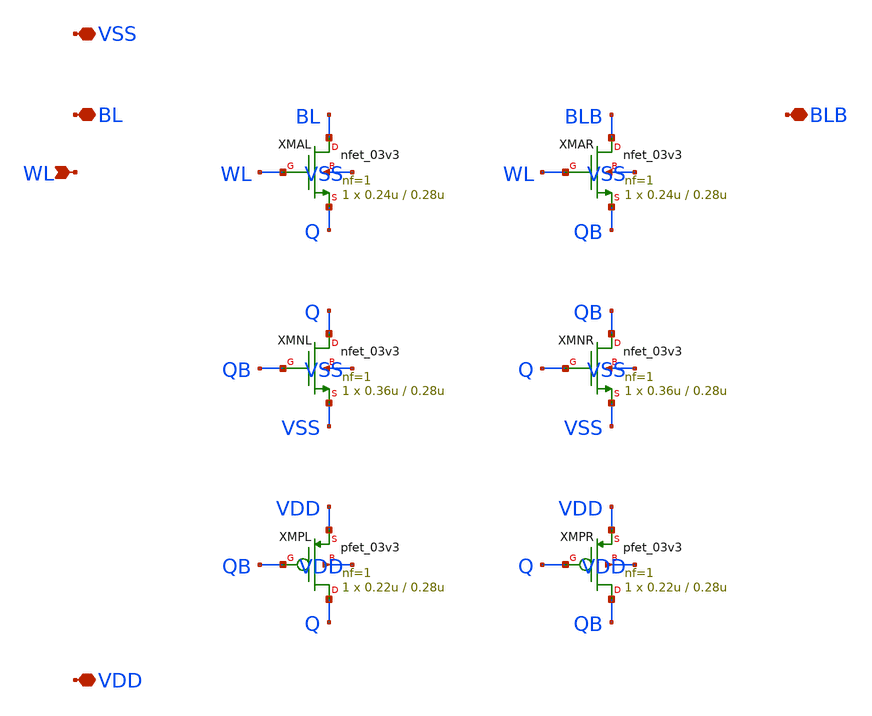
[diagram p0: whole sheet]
** sch_path: design/bitcell_6t.sch
**.subckt bitcell_6t BL BLB WL VDD VSS
*.iopin BL
*.iopin BLB
*.ipin WL
*.iopin VDD
*.iopin VSS
XMPL Q QB VDD VDD pfet_03v3 L=0.28u W=0.22u nf=1 ad='int((nf+1)/2) * W/nf * 0.18u' as='int((nf+2)/2) * W/nf * 0.18u'
+ pd='2*int((nf+1)/2) * (W/nf + 0.18u)' ps='2*int((nf+2)/2) * (W/nf + 0.18u)' nrd='0.18u / W' nrs='0.18u / W'
+ sa=0 sb=0 sd=0 m=1
XMPR QB Q VDD VDD pfet_03v3 L=0.28u W=0.22u nf=1 ad='int((nf+1)/2) * W/nf * 0.18u' as='int((nf+2)/2) * W/nf * 0.18u'
+ pd='2*int((nf+1)/2) * (W/nf + 0.18u)' ps='2*int((nf+2)/2) * (W/nf + 0.18u)' nrd='0.18u / W' nrs='0.18u / W'
+ sa=0 sb=0 sd=0 m=1
XMNL Q QB VSS VSS nfet_03v3 L=0.28u W=0.36u nf=1 ad='int((nf+1)/2) * W/nf * 0.18u' as='int((nf+2)/2) * W/nf * 0.18u'
+ pd='2*int((nf+1)/2) * (W/nf + 0.18u)' ps='2*int((nf+2)/2) * (W/nf + 0.18u)' nrd='0.18u / W' nrs='0.18u / W'
+ sa=0 sb=0 sd=0 m=1
XMNR QB Q VSS VSS nfet_03v3 L=0.28u W=0.36u nf=1 ad='int((nf+1)/2) * W/nf * 0.18u' as='int((nf+2)/2) * W/nf * 0.18u'
+ pd='2*int((nf+1)/2) * (W/nf + 0.18u)' ps='2*int((nf+2)/2) * (W/nf + 0.18u)' nrd='0.18u / W' nrs='0.18u / W'
+ sa=0 sb=0 sd=0 m=1
XMAL BL WL Q VSS nfet_03v3 L=0.28u W=0.24u nf=1 ad='int((nf+1)/2) * W/nf * 0.18u' as='int((nf+2)/2) * W/nf * 0.18u'
+ pd='2*int((nf+1)/2) * (W/nf + 0.18u)' ps='2*int((nf+2)/2) * (W/nf + 0.18u)' nrd='0.18u / W' nrs='0.18u / W'
+ sa=0 sb=0 sd=0 m=1
XMAR BLB WL QB VSS nfet_03v3 L=0.28u W=0.24u nf=1 ad='int((nf+1)/2) * W/nf * 0.18u' as='int((nf+2)/2) * W/nf * 0.18u'
+ pd='2*int((nf+1)/2) * (W/nf + 0.18u)' ps='2*int((nf+2)/2) * (W/nf + 0.18u)' nrd='0.18u / W' nrs='0.18u / W'
+ sa=0 sb=0 sd=0 m=1
**.ends
.end
